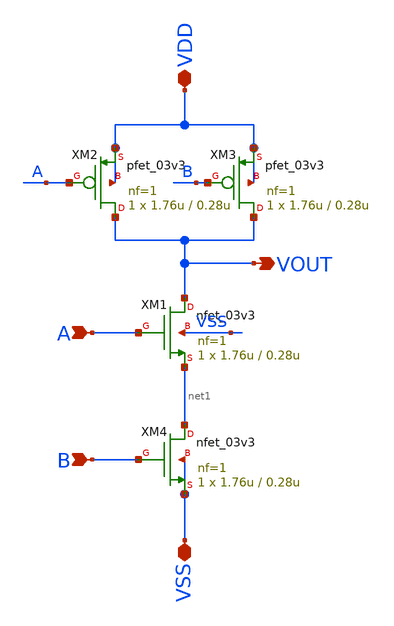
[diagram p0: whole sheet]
** sch_path: Clock_Generator_PAKISTAN_06/Xschem/strong_NAND.sch
**.subckt strong_NAND VDD VSS A B VOUT
*.iopin VDD
*.iopin VSS
*.ipin A
*.ipin B
*.opin VOUT
XM1 VOUT A net1 VSS nfet_03v3 L=0.28u W=1.76u nf=1 ad='int((nf+1)/2) * W/nf * 0.18u' as='int((nf+2)/2) * W/nf * 0.18u'
+ pd='2*int((nf+1)/2) * (W/nf + 0.18u)' ps='2*int((nf+2)/2) * (W/nf + 0.18u)' nrd='0.18u / W' nrs='0.18u / W'
+ sa=0 sb=0 sd=0 m=1
XM2 VOUT A VDD VDD pfet_03v3 L=0.28u W=1.76u nf=1 ad='int((nf+1)/2) * W/nf * 0.18u' as='int((nf+2)/2) * W/nf * 0.18u'
+ pd='2*int((nf+1)/2) * (W/nf + 0.18u)' ps='2*int((nf+2)/2) * (W/nf + 0.18u)' nrd='0.18u / W' nrs='0.18u / W'
+ sa=0 sb=0 sd=0 m=1
XM3 VOUT B VDD VDD pfet_03v3 L=0.28u W=1.76u nf=1 ad='int((nf+1)/2) * W/nf * 0.18u' as='int((nf+2)/2) * W/nf * 0.18u'
+ pd='2*int((nf+1)/2) * (W/nf + 0.18u)' ps='2*int((nf+2)/2) * (W/nf + 0.18u)' nrd='0.18u / W' nrs='0.18u / W'
+ sa=0 sb=0 sd=0 m=1
XM4 net1 B VSS VSS nfet_03v3 L=0.28u W=1.76u nf=1 ad='int((nf+1)/2) * W/nf * 0.18u' as='int((nf+2)/2) * W/nf * 0.18u'
+ pd='2*int((nf+1)/2) * (W/nf + 0.18u)' ps='2*int((nf+2)/2) * (W/nf + 0.18u)' nrd='0.18u / W' nrs='0.18u / W'
+ sa=0 sb=0 sd=0 m=1
**.ends
.end
